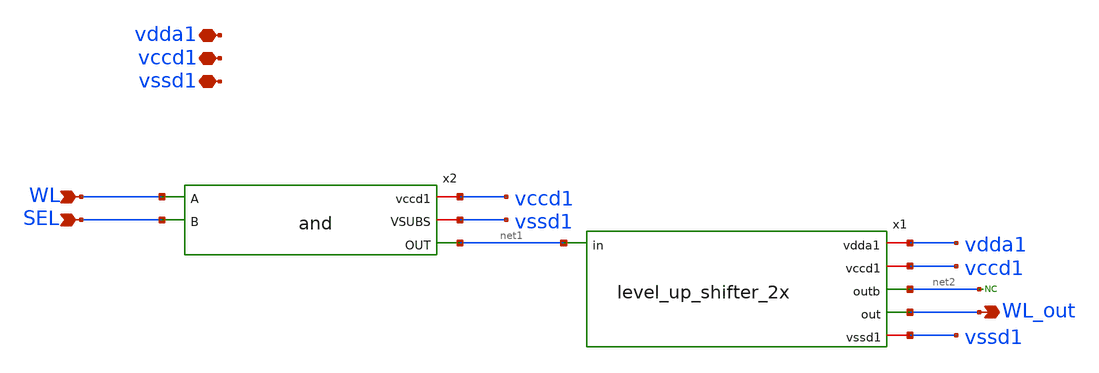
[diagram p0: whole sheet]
** sch_path: xschem/WL_driver.sch
**.subckt WL_driver vccd1 vdda1 vssd1 WL SEL WL_out
*.iopin vccd1
*.iopin vdda1
*.iopin vssd1
*.ipin WL
*.ipin SEL
*.opin WL_out
x1 vdda1 vccd1 net1 net2 WL_out vssd1 level_up_shifter_2x
x2 vccd1 vssd1 WL SEL net1 and
* noconn #net2
**.ends
.end
